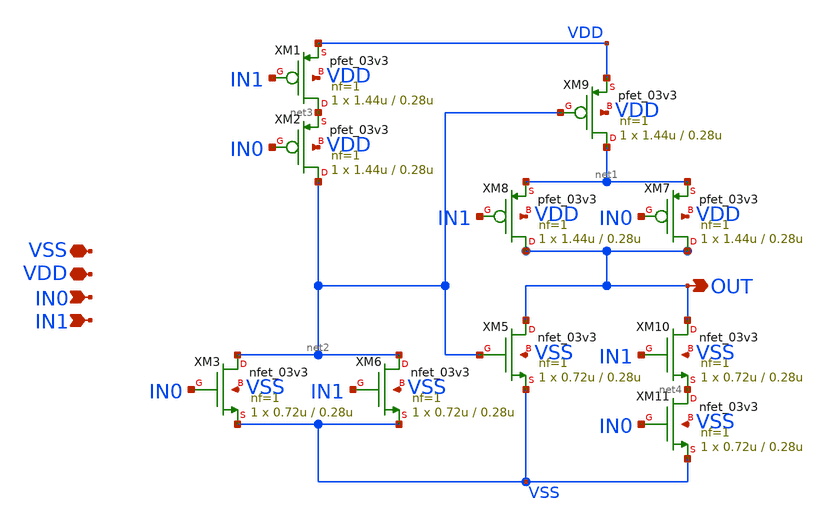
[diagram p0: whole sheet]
** sch_path: CAD4/xor2.sch
**.subckt xor2 VSS VDD IN0 IN1 OUT
*.iopin VSS
*.iopin VDD
*.ipin IN0
*.ipin IN1
*.opin OUT
XM1 net3 IN1 VDD VDD pfet_03v3 L=0.28u W=1.44u nf=1 ad='int((nf+1)/2) * W/nf * 0.18u' as='int((nf+2)/2) * W/nf * 0.18u'
+ pd='2*int((nf+1)/2) * (W/nf + 0.18u)' ps='2*int((nf+2)/2) * (W/nf + 0.18u)' nrd='0.18u / W' nrs='0.18u / W'
+ sa=0 sb=0 sd=0 m=1
XM2 net2 IN0 net3 VDD pfet_03v3 L=0.28u W=1.44u nf=1 ad='int((nf+1)/2) * W/nf * 0.18u' as='int((nf+2)/2) * W/nf * 0.18u'
+ pd='2*int((nf+1)/2) * (W/nf + 0.18u)' ps='2*int((nf+2)/2) * (W/nf + 0.18u)' nrd='0.18u / W' nrs='0.18u / W'
+ sa=0 sb=0 sd=0 m=1
XM3 net2 IN0 VSS VSS nfet_03v3 L=0.28u W=0.72u nf=1 ad='int((nf+1)/2) * W/nf * 0.18u' as='int((nf+2)/2) * W/nf * 0.18u'
+ pd='2*int((nf+1)/2) * (W/nf + 0.18u)' ps='2*int((nf+2)/2) * (W/nf + 0.18u)' nrd='0.18u / W' nrs='0.18u / W'
+ sa=0 sb=0 sd=0 m=1
XM5 OUT net2 VSS VSS nfet_03v3 L=0.28u W=0.72u nf=1 ad='int((nf+1)/2) * W/nf * 0.18u' as='int((nf+2)/2) * W/nf * 0.18u'
+ pd='2*int((nf+1)/2) * (W/nf + 0.18u)' ps='2*int((nf+2)/2) * (W/nf + 0.18u)' nrd='0.18u / W' nrs='0.18u / W'
+ sa=0 sb=0 sd=0 m=1
XM6 net2 IN1 VSS VSS nfet_03v3 L=0.28u W=0.72u nf=1 ad='int((nf+1)/2) * W/nf * 0.18u' as='int((nf+2)/2) * W/nf * 0.18u'
+ pd='2*int((nf+1)/2) * (W/nf + 0.18u)' ps='2*int((nf+2)/2) * (W/nf + 0.18u)' nrd='0.18u / W' nrs='0.18u / W'
+ sa=0 sb=0 sd=0 m=1
XM7 OUT IN0 net1 VDD pfet_03v3 L=0.28u W=1.44u nf=1 ad='int((nf+1)/2) * W/nf * 0.18u' as='int((nf+2)/2) * W/nf * 0.18u'
+ pd='2*int((nf+1)/2) * (W/nf + 0.18u)' ps='2*int((nf+2)/2) * (W/nf + 0.18u)' nrd='0.18u / W' nrs='0.18u / W'
+ sa=0 sb=0 sd=0 m=1
XM8 OUT IN1 net1 VDD pfet_03v3 L=0.28u W=1.44u nf=1 ad='int((nf+1)/2) * W/nf * 0.18u' as='int((nf+2)/2) * W/nf * 0.18u'
+ pd='2*int((nf+1)/2) * (W/nf + 0.18u)' ps='2*int((nf+2)/2) * (W/nf + 0.18u)' nrd='0.18u / W' nrs='0.18u / W'
+ sa=0 sb=0 sd=0 m=1
XM9 net1 net2 VDD VDD pfet_03v3 L=0.28u W=1.44u nf=1 ad='int((nf+1)/2) * W/nf * 0.18u' as='int((nf+2)/2) * W/nf * 0.18u'
+ pd='2*int((nf+1)/2) * (W/nf + 0.18u)' ps='2*int((nf+2)/2) * (W/nf + 0.18u)' nrd='0.18u / W' nrs='0.18u / W'
+ sa=0 sb=0 sd=0 m=1
XM10 OUT IN1 net4 VSS nfet_03v3 L=0.28u W=0.72u nf=1 ad='int((nf+1)/2) * W/nf * 0.18u' as='int((nf+2)/2) * W/nf * 0.18u'
+ pd='2*int((nf+1)/2) * (W/nf + 0.18u)' ps='2*int((nf+2)/2) * (W/nf + 0.18u)' nrd='0.18u / W' nrs='0.18u / W'
+ sa=0 sb=0 sd=0 m=1
XM11 net4 IN0 VSS VSS nfet_03v3 L=0.28u W=0.72u nf=1 ad='int((nf+1)/2) * W/nf * 0.18u' as='int((nf+2)/2) * W/nf * 0.18u'
+ pd='2*int((nf+1)/2) * (W/nf + 0.18u)' ps='2*int((nf+2)/2) * (W/nf + 0.18u)' nrd='0.18u / W' nrs='0.18u / W'
+ sa=0 sb=0 sd=0 m=1
**.ends
.end
